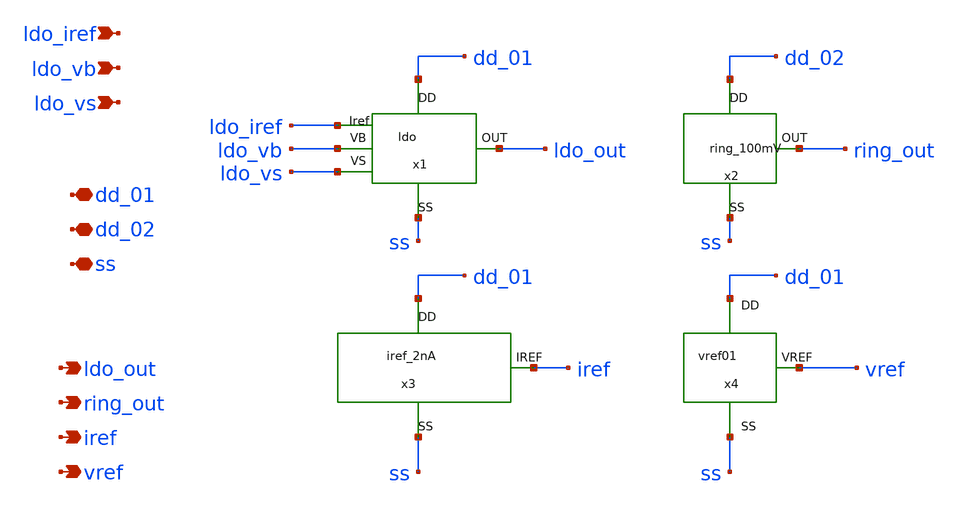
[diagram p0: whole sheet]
** sch_path: xschem/pmu_circuits.sch
**.subckt pmu_circuits dd_01 dd_02 ss ldo_out ring_out iref vref ldo_iref ldo_vb ldo_vs
*.iopin dd_01
*.iopin dd_02
*.iopin ss
*.opin ldo_out
*.opin ring_out
*.opin iref
*.opin vref
*.ipin ldo_iref
*.ipin ldo_vb
*.ipin ldo_vs
x2 ring_out dd_02 ss ring_100mV
x1 ldo_out dd_01 ss ldo_vb ldo_vs ldo_iref ldo
x3 iref dd_01 ss iref_2nA
x4 vref dd_01 ss vref01
**.ends

* expanding   symbol:  ring_100mV.sym # of pins=3
** sym_path: xschem/ring_100mV.sym
** sch_path: xschem/ring_100mV.sch
.subckt ring_100mV OUT DD SS
*.iopin DD
*.iopin SS
*.opin OUT
X2 net1 net2 DD SS mdls_inv
X1 net2 net3 DD SS mdls_inv
X3 net3 net4 DD SS mdls_inv
X4 net4 out_aux DD SS mdls_inv
X10 out_aux net5 DD SS mdls_inv
X11 net5 net6 DD SS mdls_inv
X12 net6 net7 DD SS mdls_inv
X13 net7 net8 DD SS mdls_inv
X14 net8 net1 DD SS mdls_inv
X5 out_aux net9 DD SS mdls_inv
X6 net9 OUT DD SS ring_100mV_buffer
.ends


* expanding   symbol:  ldo.sym # of pins=6
** sym_path: xschem/ldo.sym
** sch_path: xschem/ldo.sch
.subckt ldo OUT DD SS VB VS Iref
*.iopin DD
*.ipin Iref
*.opin OUT
*.ipin VB
*.ipin VS
*.iopin SS
XMN1 net3 VB net1 SS sky130_fd_pr__nfet_01v8_lvt L=1.43 W=5.19 nf=1 ad='int((nf+1)/2) * W/nf * 0.29'
+ as='int((nf+2)/2) * W/nf * 0.29' pd='2*int((nf+1)/2) * (W/nf + 0.29)' ps='2*int((nf+2)/2) * (W/nf + 0.29)'
+ nrd='0.29 / W' nrs='0.29 / W' sa=0 sb=0 sd=0 mult=2 m=2
XMN2c net1 Iref SS SS sky130_fd_pr__nfet_01v8_lvt L=0.66 W=5.10 nf=1 ad='int((nf+1)/2) * W/nf * 0.29'
+ as='int((nf+2)/2) * W/nf * 0.29' pd='2*int((nf+1)/2) * (W/nf + 0.29)' ps='2*int((nf+2)/2) * (W/nf + 0.29)'
+ nrd='0.29 / W' nrs='0.29 / W' sa=0 sb=0 sd=0 mult=4 m=4
XMN2b net2 Iref SS SS sky130_fd_pr__nfet_01v8_lvt L=0.66 W=5.10 nf=1 ad='int((nf+1)/2) * W/nf * 0.29'
+ as='int((nf+2)/2) * W/nf * 0.29' pd='2*int((nf+1)/2) * (W/nf + 0.29)' ps='2*int((nf+2)/2) * (W/nf + 0.29)'
+ nrd='0.29 / W' nrs='0.29 / W' sa=0 sb=0 sd=0 mult=2 m=2
XMN2a Iref Iref SS SS sky130_fd_pr__nfet_01v8_lvt L=0.66 W=5.10 nf=1 ad='int((nf+1)/2) * W/nf * 0.29'
+ as='int((nf+2)/2) * W/nf * 0.29' pd='2*int((nf+1)/2) * (W/nf + 0.29)' ps='2*int((nf+2)/2) * (W/nf + 0.29)'
+ nrd='0.29 / W' nrs='0.29 / W' sa=0 sb=0 sd=0 mult=2 m=2
XMP2 net1 VS OUT OUT sky130_fd_pr__pfet_01v8_lvt L=1.27 W=6.07 nf=1 ad='int((nf+1)/2) * W/nf * 0.29'
+ as='int((nf+2)/2) * W/nf * 0.29' pd='2*int((nf+1)/2) * (W/nf + 0.29)' ps='2*int((nf+2)/2) * (W/nf + 0.29)'
+ nrd='0.29 / W' nrs='0.29 / W' sa=0 sb=0 sd=0 mult=2 m=2
XMP1 OUT net3 DD DD sky130_fd_pr__pfet_01v8_lvt L=0.37 W=5.17 nf=1 ad='int((1 + 1)/2) * 5.17 / 1 * 0.29'
+ as='int((1 + 2)/2) * 5.17 / 1 * 0.29' pd='2*int((1 + 1)/2) * (5.17 / 1 + 0.29)' ps='2*int((1 + 2)/2) * (5.17 / 1 + 0.29)'
+ nrd='0.29 / 5.17 ' nrs='0.29 / 5.17 ' sa=0 sb=0 sd=0 mult=1 m=1
XMP3b net3 net2 DD DD sky130_fd_pr__pfet_01v8 L=3.89 W=0.89 nf=1 ad='int((nf+1)/2) * W/nf * 0.29' as='int((nf+2)/2) * W/nf * 0.29'
+ pd='2*int((nf+1)/2) * (W/nf + 0.29)' ps='2*int((nf+2)/2) * (W/nf + 0.29)' nrd='0.29 / W' nrs='0.29 / W'
+ sa=0 sb=0 sd=0 mult=2 m=2
XMP3a net2 net2 DD DD sky130_fd_pr__pfet_01v8 L=3.89 W=0.89 nf=1 ad='int((nf+1)/2) * W/nf * 0.29' as='int((nf+2)/2) * W/nf * 0.29'
+ pd='2*int((nf+1)/2) * (W/nf + 0.29)' ps='2*int((nf+2)/2) * (W/nf + 0.29)' nrd='0.29 / W' nrs='0.29 / W'
+ sa=0 sb=0 sd=0 mult=2 m=2
XC1 net3 OUT sky130_fd_pr__cap_mim_m3_1 W=4 L=15 MF=1 m=1
XMP3 DD DD DD DD sky130_fd_pr__pfet_01v8 L=3.89 W=0.89 nf=1 ad='int((nf+1)/2) * W/nf * 0.29' as='int((nf+2)/2) * W/nf * 0.29'
+ pd='2*int((nf+1)/2) * (W/nf + 0.29)' ps='2*int((nf+2)/2) * (W/nf + 0.29)' nrd='0.29 / W' nrs='0.29 / W'
+ sa=0 sb=0 sd=0 mult=2 m=2
XMN2 SS SS SS SS sky130_fd_pr__nfet_01v8_lvt L=0.66 W=5.10 nf=1 ad='int((nf+1)/2) * W/nf * 0.29' as='int((nf+2)/2) * W/nf * 0.29'
+ pd='2*int((nf+1)/2) * (W/nf + 0.29)' ps='2*int((nf+2)/2) * (W/nf + 0.29)' nrd='0.29 / W' nrs='0.29 / W'
+ sa=0 sb=0 sd=0 mult=2 m=2
.ends


* expanding   symbol:  iref_2nA.sym # of pins=3
** sym_path: xschem/iref_2nA.sym
** sch_path: xschem/iref_2nA.sch
.subckt iref_2nA IREF DD SS
*.iopin DD
*.iopin SS
*.iopin IREF
x1 net3 SS net1 VCTAT net2 iref_2nA_igenerator
x3 DD SS net1 net2 net3 IREF iref_2nA_mirrors
x2 VCTAT DD SS iref_2nA_vref
.ends


* expanding   symbol:  vref01.sym # of pins=3
** sym_path: xschem/vref01.sym
** sch_path: xschem/vref01.sch
.subckt vref01 VREF DD SS
*.opin VREF
*.iopin SS
*.iopin DD
XM1 DD gate gate SS sky130_fd_pr__nfet_01v8_lvt L=0.89 W=6 nf=1 ad='int((nf+1)/2) * W/nf * 0.29' as='int((nf+2)/2) * W/nf * 0.29'
+ pd='2*int((nf+1)/2) * (W/nf + 0.29)' ps='2*int((nf+2)/2) * (W/nf + 0.29)' nrd='0.29 / W' nrs='0.29 / W'
+ sa=0 sb=0 sd=0 mult=2 m=2
XM2 gate gate VREF SS sky130_fd_pr__nfet_01v8_lvt L=3.10 W=1.72 nf=1 ad='int((nf+1)/2) * W/nf * 0.29'
+ as='int((nf+2)/2) * W/nf * 0.29' pd='2*int((nf+1)/2) * (W/nf + 0.29)' ps='2*int((nf+2)/2) * (W/nf + 0.29)'
+ nrd='0.29 / W' nrs='0.29 / W' sa=0 sb=0 sd=0 mult=1 m=1
XM3 VREF gate SS SS sky130_fd_pr__nfet_01v8 L=1.05 W=0.82 nf=1 ad='int((nf+1)/2) * W/nf * 0.29' as='int((nf+2)/2) * W/nf * 0.29'
+ pd='2*int((nf+1)/2) * (W/nf + 0.29)' ps='2*int((nf+2)/2) * (W/nf + 0.29)' nrd='0.29 / W' nrs='0.29 / W'
+ sa=0 sb=0 sd=0 mult=1 m=1
D1 VREF DD sky130_fd_pr__diode_pd2nw_05v5_lvt area=4.225e+11
.ends


* expanding   symbol:  mdls_inv.sym # of pins=4
** sym_path: xschem/mdls_inv.sym
** sch_path: xschem/mdls_inv.sch
.subckt mdls_inv IN OUT DD SS
*.ipin IN
*.iopin DD
*.iopin SS
*.opin OUT
XM5 OUT IN net1 SS sky130_fd_pr__nfet_01v8_lvt L=0.8 W=5.5 nf=1 ad='int((nf+1)/2) * W/nf * 0.29' as='int((nf+2)/2) * W/nf * 0.29'
+ pd='2*int((nf+1)/2) * (W/nf + 0.29)' ps='2*int((nf+2)/2) * (W/nf + 0.29)' nrd='0.29 / W' nrs='0.29 / W'
+ sa=0 sb=0 sd=0 mult=4 m=4
XM10 OUT IN net2 DD sky130_fd_pr__pfet_01v8_lvt L=0.8 W=1 nf=1 ad='int((nf+1)/2) * W/nf * 0.29' as='int((nf+2)/2) * W/nf * 0.29'
+ pd='2*int((nf+1)/2) * (W/nf + 0.29)' ps='2*int((nf+2)/2) * (W/nf + 0.29)' nrd='0.29 / W' nrs='0.29 / W'
+ sa=0 sb=0 sd=0 mult=1 m=1
XM11 net1 IN SS SS sky130_fd_pr__nfet_01v8_lvt L=1 W=5.5 nf=1 ad='int((nf+1)/2) * W/nf * 0.29' as='int((nf+2)/2) * W/nf * 0.29'
+ pd='2*int((nf+1)/2) * (W/nf + 0.29)' ps='2*int((nf+2)/2) * (W/nf + 0.29)' nrd='0.29 / W' nrs='0.29 / W'
+ sa=0 sb=0 sd=0 mult=2 m=2
XM13 net2 IN DD DD sky130_fd_pr__pfet_01v8_lvt L=2 W=1 nf=1 ad='int((nf+1)/2) * W/nf * 0.29' as='int((nf+2)/2) * W/nf * 0.29'
+ pd='2*int((nf+1)/2) * (W/nf + 0.29)' ps='2*int((nf+2)/2) * (W/nf + 0.29)' nrd='0.29 / W' nrs='0.29 / W'
+ sa=0 sb=0 sd=0 mult=1 m=1
XM1 net1 OUT SS DD sky130_fd_pr__pfet_01v8_lvt L=0.8 W=1 nf=1 ad='int((nf+1)/2) * W/nf * 0.29' as='int((nf+2)/2) * W/nf * 0.29'
+ pd='2*int((nf+1)/2) * (W/nf + 0.29)' ps='2*int((nf+2)/2) * (W/nf + 0.29)' nrd='0.29 / W' nrs='0.29 / W'
+ sa=0 sb=0 sd=0 mult=1 m=1
XM2 net2 OUT DD SS sky130_fd_pr__nfet_01v8_lvt L=0.4 W=5.5 nf=1 ad='int((nf+1)/2) * W/nf * 0.29' as='int((nf+2)/2) * W/nf * 0.29'
+ pd='2*int((nf+1)/2) * (W/nf + 0.29)' ps='2*int((nf+2)/2) * (W/nf + 0.29)' nrd='0.29 / W' nrs='0.29 / W'
+ sa=0 sb=0 sd=0 mult=2 m=2
.ends


* expanding   symbol:  ring_100mV_buffer.sym # of pins=4
** sym_path: xschem/ring_100mV_buffer.sym
** sch_path: xschem/ring_100mV_buffer.sch
.subckt ring_100mV_buffer IN OUT DD SS
*.opin OUT
*.iopin DD
*.iopin SS
*.ipin IN
XM5 net1 IN SS SS sky130_fd_pr__nfet_01v8_lvt L=0.8 W=5.5 nf=1 ad='int((nf+1)/2) * W/nf * 0.29' as='int((nf+2)/2) * W/nf * 0.29'
+ pd='2*int((nf+1)/2) * (W/nf + 0.29)' ps='2*int((nf+2)/2) * (W/nf + 0.29)' nrd='0.29 / W' nrs='0.29 / W'
+ sa=0 sb=0 sd=0 mult=8 m=8
XM10 net1 IN DD DD sky130_fd_pr__pfet_01v8_lvt L=0.8 W=1 nf=1 ad='int((nf+1)/2) * W/nf * 0.29' as='int((nf+2)/2) * W/nf * 0.29'
+ pd='2*int((nf+1)/2) * (W/nf + 0.29)' ps='2*int((nf+2)/2) * (W/nf + 0.29)' nrd='0.29 / W' nrs='0.29 / W'
+ sa=0 sb=0 sd=0 mult=2 m=2
XM1 OUT net1 SS SS sky130_fd_pr__nfet_01v8_lvt L=0.8 W=5.5 nf=1 ad='int((nf+1)/2) * W/nf * 0.29' as='int((nf+2)/2) * W/nf * 0.29'
+ pd='2*int((nf+1)/2) * (W/nf + 0.29)' ps='2*int((nf+2)/2) * (W/nf + 0.29)' nrd='0.29 / W' nrs='0.29 / W'
+ sa=0 sb=0 sd=0 mult=16 m=16
XM2 OUT net1 DD DD sky130_fd_pr__pfet_01v8_lvt L=0.8 W=1 nf=1 ad='int((nf+1)/2) * W/nf * 0.29' as='int((nf+2)/2) * W/nf * 0.29'
+ pd='2*int((nf+1)/2) * (W/nf + 0.29)' ps='2*int((nf+2)/2) * (W/nf + 0.29)' nrd='0.29 / W' nrs='0.29 / W'
+ sa=0 sb=0 sd=0 mult=4 m=4
.ends


* expanding   symbol:  iref_2nA_igenerator.sym # of pins=5
** sym_path: xschem/iref_2nA_igenerator.sym
** sch_path: xschem/iref_2nA_igenerator.sch
.subckt iref_2nA_igenerator Ip2 SS Ip1 VCTAT Vg
*.iopin SS
*.ipin VCTAT
*.iopin Ip1
*.iopin Vg
*.iopin Ip2
XM1 Ip1 Vg VPTAT SS sky130_fd_pr__nfet_01v8_lvt L=1 W=2.5 nf=1 ad='int((nf+1)/2) * W/nf * 0.29' as='int((nf+2)/2) * W/nf * 0.29'
+ pd='2*int((nf+1)/2) * (W/nf + 0.29)' ps='2*int((nf+2)/2) * (W/nf + 0.29)' nrd='0.29 / W' nrs='0.29 / W'
+ sa=0 sb=0 sd=0 mult=2 m=2
XM2 Ip2 Vg SS SS sky130_fd_pr__nfet_01v8_lvt L=1 W=2.5 nf=1 ad='int((nf+1)/2) * W/nf * 0.29' as='int((nf+2)/2) * W/nf * 0.29'
+ pd='2*int((nf+1)/2) * (W/nf + 0.29)' ps='2*int((nf+2)/2) * (W/nf + 0.29)' nrd='0.29 / W' nrs='0.29 / W'
+ sa=0 sb=0 sd=0 mult=2 m=2
XM3 VPTAT VCTAT SS SS sky130_fd_pr__nfet_01v8_lvt L=5 W=1 nf=1 ad='int((nf+1)/2) * W/nf * 0.29' as='int((nf+2)/2) * W/nf * 0.29'
+ pd='2*int((nf+1)/2) * (W/nf + 0.29)' ps='2*int((nf+2)/2) * (W/nf + 0.29)' nrd='0.29 / W' nrs='0.29 / W'
+ sa=0 sb=0 sd=0 mult=1 m=1
XM4 SS SS SS SS sky130_fd_pr__nfet_01v8_lvt L=1 W=2.5 nf=1 ad='int((nf+1)/2) * W/nf * 0.29' as='int((nf+2)/2) * W/nf * 0.29'
+ pd='2*int((nf+1)/2) * (W/nf + 0.29)' ps='2*int((nf+2)/2) * (W/nf + 0.29)' nrd='0.29 / W' nrs='0.29 / W'
+ sa=0 sb=0 sd=0 mult=2 m=2
.ends


* expanding   symbol:  iref_2nA_mirrors.sym # of pins=6
** sym_path: xschem/iref_2nA_mirrors.sym
** sch_path: xschem/iref_2nA_mirrors.sch
.subckt iref_2nA_mirrors DD SS Ip1 Vg Ip2 Iref
*.iopin DD
*.iopin SS
*.iopin Iref
*.iopin Ip2
*.iopin Vg
*.iopin Ip1
XM7 net3 Ip2 DD DD sky130_fd_pr__pfet_01v8_lvt L=2 W=2.5 nf=1 ad='int((nf+1)/2) * W/nf * 0.29' as='int((nf+2)/2) * W/nf * 0.29'
+ pd='2*int((nf+1)/2) * (W/nf + 0.29)' ps='2*int((nf+2)/2) * (W/nf + 0.29)' nrd='0.29 / W' nrs='0.29 / W'
+ sa=0 sb=0 sd=0 mult=10 m=10
XM8 net2 Ip1 DD DD sky130_fd_pr__pfet_01v8_lvt L=2 W=2.5 nf=1 ad='int((nf+1)/2) * W/nf * 0.29' as='int((nf+2)/2) * W/nf * 0.29'
+ pd='2*int((nf+1)/2) * (W/nf + 0.29)' ps='2*int((nf+2)/2) * (W/nf + 0.29)' nrd='0.29 / W' nrs='0.29 / W'
+ sa=0 sb=0 sd=0 mult=2 m=2
XM9 net4 Ip2 DD DD sky130_fd_pr__pfet_01v8_lvt L=2 W=2.5 nf=1 ad='int((nf+1)/2) * W/nf * 0.29' as='int((nf+2)/2) * W/nf * 0.29'
+ pd='2*int((nf+1)/2) * (W/nf + 0.29)' ps='2*int((nf+2)/2) * (W/nf + 0.29)' nrd='0.29 / W' nrs='0.29 / W'
+ sa=0 sb=0 sd=0 mult=2 m=2
XM10 net1 Ip1 DD DD sky130_fd_pr__pfet_01v8_lvt L=2 W=2.5 nf=1 ad='int((nf+1)/2) * W/nf * 0.29' as='int((nf+2)/2) * W/nf * 0.29'
+ pd='2*int((nf+1)/2) * (W/nf + 0.29)' ps='2*int((nf+2)/2) * (W/nf + 0.29)' nrd='0.29 / W' nrs='0.29 / W'
+ sa=0 sb=0 sd=0 mult=2 m=2
XM11 Vn Vn SS SS sky130_fd_pr__nfet_01v8_lvt L=1 W=2.5 nf=1 ad='int((nf+1)/2) * W/nf * 0.29' as='int((nf+2)/2) * W/nf * 0.29'
+ pd='2*int((nf+1)/2) * (W/nf + 0.29)' ps='2*int((nf+2)/2) * (W/nf + 0.29)' nrd='0.29 / W' nrs='0.29 / W'
+ sa=0 sb=0 sd=0 mult=2 m=2
XM12 Vg Vn SS SS sky130_fd_pr__nfet_01v8_lvt L=1 W=2.5 nf=1 ad='int((nf+1)/2) * W/nf * 0.29' as='int((nf+2)/2) * W/nf * 0.29'
+ pd='2*int((nf+1)/2) * (W/nf + 0.29)' ps='2*int((nf+2)/2) * (W/nf + 0.29)' nrd='0.29 / W' nrs='0.29 / W'
+ sa=0 sb=0 sd=0 mult=2 m=2
XM15 net5 Ip2 DD DD sky130_fd_pr__pfet_01v8_lvt L=2 W=2.5 nf=1 ad='int((nf+1)/2) * W/nf * 0.29' as='int((nf+2)/2) * W/nf * 0.29'
+ pd='2*int((nf+1)/2) * (W/nf + 0.29)' ps='2*int((nf+2)/2) * (W/nf + 0.29)' nrd='0.29 / W' nrs='0.29 / W'
+ sa=0 sb=0 sd=0 mult=2 m=2
XM16 Vg Vb net2 DD sky130_fd_pr__pfet_01v8_lvt L=2 W=2.5 nf=1 ad='int((nf+1)/2) * W/nf * 0.29' as='int((nf+2)/2) * W/nf * 0.29'
+ pd='2*int((nf+1)/2) * (W/nf + 0.29)' ps='2*int((nf+2)/2) * (W/nf + 0.29)' nrd='0.29 / W' nrs='0.29 / W'
+ sa=0 sb=0 sd=0 mult=2 m=2
XM17 Ip1 Vb net1 DD sky130_fd_pr__pfet_01v8_lvt L=2 W=2.5 nf=1 ad='int((nf+1)/2) * W/nf * 0.29' as='int((nf+2)/2) * W/nf * 0.29'
+ pd='2*int((nf+1)/2) * (W/nf + 0.29)' ps='2*int((nf+2)/2) * (W/nf + 0.29)' nrd='0.29 / W' nrs='0.29 / W'
+ sa=0 sb=0 sd=0 mult=2 m=2
XM18 Ip2 Vb net3 DD sky130_fd_pr__pfet_01v8_lvt L=2 W=2.5 nf=1 ad='int((nf+1)/2) * W/nf * 0.29' as='int((nf+2)/2) * W/nf * 0.29'
+ pd='2*int((nf+1)/2) * (W/nf + 0.29)' ps='2*int((nf+2)/2) * (W/nf + 0.29)' nrd='0.29 / W' nrs='0.29 / W'
+ sa=0 sb=0 sd=0 mult=10 m=10
XM19 Vn Vb net4 DD sky130_fd_pr__pfet_01v8_lvt L=2 W=2.5 nf=1 ad='int((nf+1)/2) * W/nf * 0.29' as='int((nf+2)/2) * W/nf * 0.29'
+ pd='2*int((nf+1)/2) * (W/nf + 0.29)' ps='2*int((nf+2)/2) * (W/nf + 0.29)' nrd='0.29 / W' nrs='0.29 / W'
+ sa=0 sb=0 sd=0 mult=2 m=2
XM20 Iref Vb net5 DD sky130_fd_pr__pfet_01v8_lvt L=2 W=2.5 nf=1 ad='int((nf+1)/2) * W/nf * 0.29' as='int((nf+2)/2) * W/nf * 0.29'
+ pd='2*int((nf+1)/2) * (W/nf + 0.29)' ps='2*int((nf+2)/2) * (W/nf + 0.29)' nrd='0.29 / W' nrs='0.29 / W'
+ sa=0 sb=0 sd=0 mult=2 m=2
XM22 net6 net6 DD DD sky130_fd_pr__pfet_01v8_lvt L=2 W=2.5 nf=1 ad='int((nf+1)/2) * W/nf * 0.29' as='int((nf+2)/2) * W/nf * 0.29'
+ pd='2*int((nf+1)/2) * (W/nf + 0.29)' ps='2*int((nf+2)/2) * (W/nf + 0.29)' nrd='0.29 / W' nrs='0.29 / W'
+ sa=0 sb=0 sd=0 mult=2 m=2
XM21 Vb Vn SS SS sky130_fd_pr__nfet_01v8_lvt L=1 W=2.5 nf=1 ad='int((nf+1)/2) * W/nf * 0.29' as='int((nf+2)/2) * W/nf * 0.29'
+ pd='2*int((nf+1)/2) * (W/nf + 0.29)' ps='2*int((nf+2)/2) * (W/nf + 0.29)' nrd='0.29 / W' nrs='0.29 / W'
+ sa=0 sb=0 sd=0 mult=2 m=2
XM23 Vb Vb net6 DD sky130_fd_pr__pfet_01v8_lvt L=2 W=2.5 nf=1 ad='int((nf+1)/2) * W/nf * 0.29' as='int((nf+2)/2) * W/nf * 0.29'
+ pd='2*int((nf+1)/2) * (W/nf + 0.29)' ps='2*int((nf+2)/2) * (W/nf + 0.29)' nrd='0.29 / W' nrs='0.29 / W'
+ sa=0 sb=0 sd=0 mult=2 m=2
XM1 DD DD DD DD sky130_fd_pr__pfet_01v8_lvt L=2 W=0.5 nf=1 ad='int((nf+1)/2) * W/nf * 0.29' as='int((nf+2)/2) * W/nf * 0.29'
+ pd='2*int((nf+1)/2) * (W/nf + 0.29)' ps='2*int((nf+2)/2) * (W/nf + 0.29)' nrd='0.29 / W' nrs='0.29 / W'
+ sa=0 sb=0 sd=0 mult=8 m=8
XM2 SS SS SS SS sky130_fd_pr__nfet_01v8_lvt L=1 W=2.5 nf=1 ad='int((nf+1)/2) * W/nf * 0.29' as='int((nf+2)/2) * W/nf * 0.29'
+ pd='2*int((nf+1)/2) * (W/nf + 0.29)' ps='2*int((nf+2)/2) * (W/nf + 0.29)' nrd='0.29 / W' nrs='0.29 / W'
+ sa=0 sb=0 sd=0 mult=2 m=2
.ends


* expanding   symbol:  iref_2nA_vref.sym # of pins=3
** sym_path: xschem/iref_2nA_vref.sym
** sch_path: xschem/iref_2nA_vref.sch
.subckt iref_2nA_vref VREF DD SS
*.iopin DD
*.iopin SS
*.iopin VREF
XM1 N2 N1 DD DD sky130_fd_pr__pfet_01v8 L=4.38 W=2.37 nf=1 ad='int((nf+1)/2) * W/nf * 0.29' as='int((nf+2)/2) * W/nf * 0.29'
+ pd='2*int((nf+1)/2) * (W/nf + 0.29)' ps='2*int((nf+2)/2) * (W/nf + 0.29)' nrd='0.29 / W' nrs='0.29 / W'
+ sa=0 sb=0 sd=0 mult=1 m=1
XM2 SS N2 N2 N2 sky130_fd_pr__pfet_01v8_lvt L=6.97 W=0.88 nf=1 ad='int((nf+1)/2) * W/nf * 0.29' as='int((nf+2)/2) * W/nf * 0.29'
+ pd='2*int((nf+1)/2) * (W/nf + 0.29)' ps='2*int((nf+2)/2) * (W/nf + 0.29)' nrd='0.29 / W' nrs='0.29 / W'
+ sa=0 sb=0 sd=0 mult=1 m=1
XM3 N1 DD DD DD sky130_fd_pr__pfet_01v8_lvt L=4 W=0.5 nf=1 ad='int((nf+1)/2) * W/nf * 0.29' as='int((nf+2)/2) * W/nf * 0.29'
+ pd='2*int((nf+1)/2) * (W/nf + 0.29)' ps='2*int((nf+2)/2) * (W/nf + 0.29)' nrd='0.29 / W' nrs='0.29 / W'
+ sa=0 sb=0 sd=0 mult=1 m=1
XM4 VREF N2 N1 DD sky130_fd_pr__pfet_01v8_lvt L=2.77 W=3.43 nf=1 ad='int((nf+1)/2) * W/nf * 0.29' as='int((nf+2)/2) * W/nf * 0.29'
+ pd='2*int((nf+1)/2) * (W/nf + 0.29)' ps='2*int((nf+2)/2) * (W/nf + 0.29)' nrd='0.29 / W' nrs='0.29 / W'
+ sa=0 sb=0 sd=0 mult=1 m=1
XM5 SS SS VREF VREF sky130_fd_pr__pfet_01v8 L=0.5 W=2 nf=1 ad='int((nf+1)/2) * W/nf * 0.29' as='int((nf+2)/2) * W/nf * 0.29'
+ pd='2*int((nf+1)/2) * (W/nf + 0.29)' ps='2*int((nf+2)/2) * (W/nf + 0.29)' nrd='0.29 / W' nrs='0.29 / W'
+ sa=0 sb=0 sd=0 mult=4 m=4
.ends

.end
